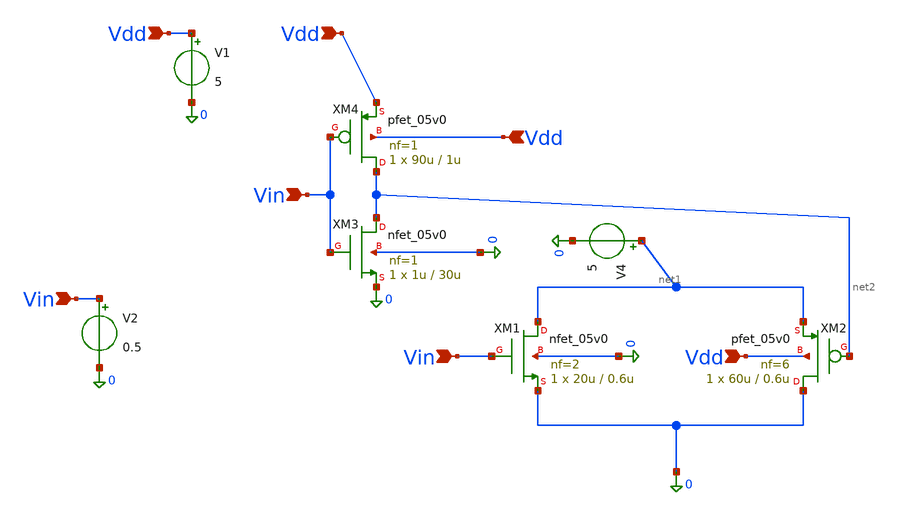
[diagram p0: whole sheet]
** sch_path: MG_switch/switch.sch
**.subckt switch Vdd Vdd Vdd Vin Vin Vin Vdd
*.ipin Vdd
*.ipin Vdd
*.ipin Vdd
*.ipin Vin
*.ipin Vin
*.ipin Vin
*.ipin Vdd
XM1 net1 Vin 0 0 nfet_05v0 L=0.6u W=20u nf=2 ad='int((nf+1)/2) * W/nf * 0.18u' as='int((nf+2)/2) * W/nf * 0.18u'
+ pd='2*int((nf+1)/2) * (W/nf + 0.18u)' ps='2*int((nf+2)/2) * (W/nf + 0.18u)' nrd='0.18u / W' nrs='0.18u / W'
+ sa=0 sb=0 sd=0 m=1
XM2 0 net2 net1 Vdd pfet_05v0 L=0.6u W=60u nf=6 ad='int((nf+1)/2) * W/nf * 0.18u' as='int((nf+2)/2) * W/nf * 0.18u'
+ pd='2*int((nf+1)/2) * (W/nf + 0.18u)' ps='2*int((nf+2)/2) * (W/nf + 0.18u)' nrd='0.18u / W' nrs='0.18u / W'
+ sa=0 sb=0 sd=0 m=1
XM3 net2 Vin 0 0 nfet_05v0 L=30u W=1u nf=1 ad='int((nf+1)/2) * W/nf * 0.18u' as='int((nf+2)/2) * W/nf * 0.18u'
+ pd='2*int((nf+1)/2) * (W/nf + 0.18u)' ps='2*int((nf+2)/2) * (W/nf + 0.18u)' nrd='0.18u / W' nrs='0.18u / W'
+ sa=0 sb=0 sd=0 m=1
XM4 net2 Vin Vdd Vdd pfet_05v0 L=1u W=90u nf=1 ad='int((nf+1)/2) * W/nf * 0.18u' as='int((nf+2)/2) * W/nf * 0.18u'
+ pd='2*int((nf+1)/2) * (W/nf + 0.18u)' ps='2*int((nf+2)/2) * (W/nf + 0.18u)' nrd='0.18u / W' nrs='0.18u / W'
+ sa=0 sb=0 sd=0 m=1
V1 Vdd 0 5
V2 Vin 0 0.5
V4 net1 0 5
**** begin user architecture code


.include /foss/pdks/gf180mcuD/libs.tech/ngspice/design.ngspice
.lib /foss/pdks/gf180mcuD/libs.tech/ngspice/sm141064.ngspice typical
.tran 0.1n 20u

**** end user architecture code
**.ends
.end
